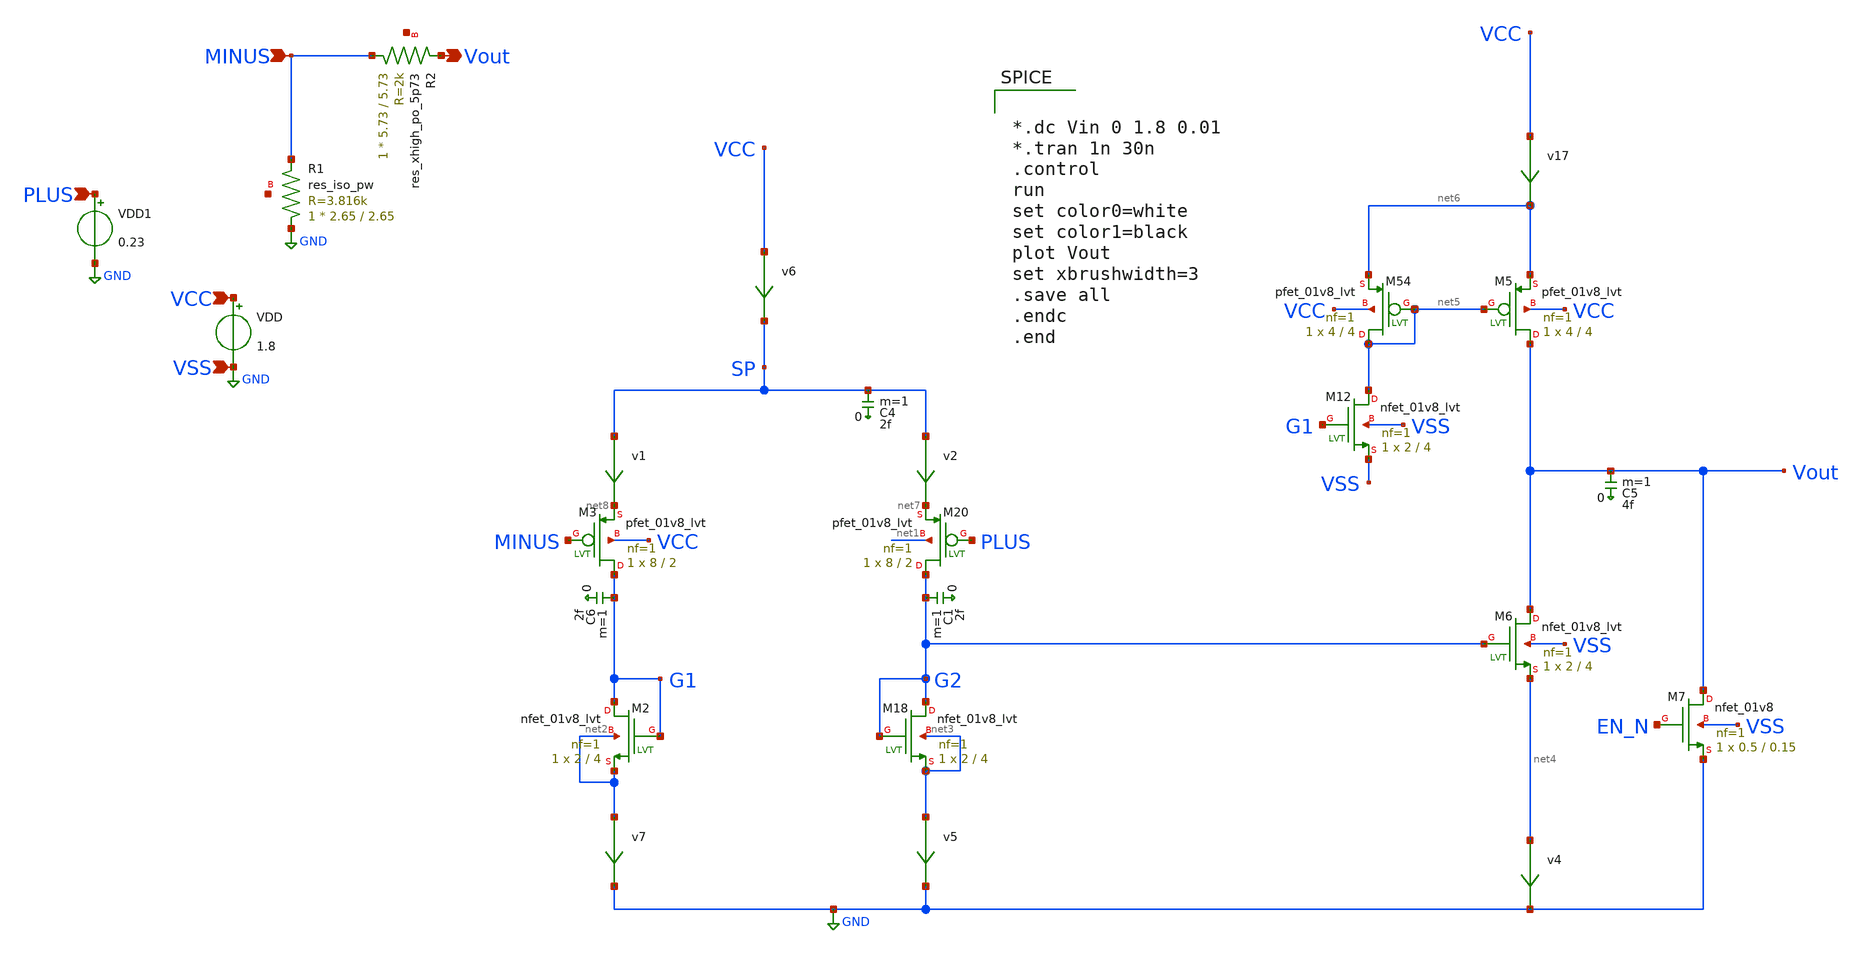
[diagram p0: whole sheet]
** sch_path: xschem/Vth_sch/Pre_layout/untitled.sch
**.subckt untitled PLUS MINUS VSS VCC Vout
*.ipin PLUS
*.ipin MINUS
*.ipin VSS
*.ipin VCC
*.opin Vout
C6 G1 0 2f m=1
XM18 G2 G2 net3 net3 sky130_fd_pr__nfet_01v8_lvt L=4 W=2 nf=1 ad='W * 0.29' as='W * 0.29' pd='2*(W + 0.29)'
+ ps='2*(W + 0.29)' nrd=0 nrs=0 sa=0 sb=0 sd=0 mult=1 m=1
XM2 G1 G1 net2 net2 sky130_fd_pr__nfet_01v8_lvt L=4 W=2 nf=1 ad='W * 0.29' as='W * 0.29' pd='2*(W + 0.29)'
+ ps='2*(W + 0.29)' nrd=0 nrs=0 sa=0 sb=0 sd=0 mult=1 m=1
XM20 G2 PLUS net7 net1 sky130_fd_pr__pfet_01v8_lvt L=2 W=8 nf=1 ad='W * 0.29' as='W * 0.29' pd='2*(W + 0.29)'
+ ps='2*(W + 0.29)' nrd=0 nrs=0 sa=0 sb=0 sd=0 mult=1 m=1
XM3 G1 MINUS net8 VCC sky130_fd_pr__pfet_01v8_lvt L=2 W=8 nf=1 ad='W * 0.29' as='W * 0.29' pd='2*(W + 0.29)'
+ ps='2*(W + 0.29)' nrd=0 nrs=0 sa=0 sb=0 sd=0 mult=1 m=1
v1 SP net8 0
.save i(v1)
C4 SP 0 2f m=1
C1 G2 0 2f m=1
C5 Vout 0 4f m=1
XM6 Vout G2 net4 VSS sky130_fd_pr__nfet_01v8_lvt L=4 W=2 nf=1 ad='W * 0.29' as='W * 0.29' pd='2*(W + 0.29)'
+ ps='2*(W + 0.29)' nrd=0 nrs=0 sa=0 sb=0 sd=0 mult=1 m=1
v2 SP net7 0
.save i(v2)
v4 net4 GND 0
.save i(v4)
v6 VCC SP 0
.save i(v6)
XM7 Vout EN_N GND VSS sky130_fd_pr__nfet_01v8 L=0.15 W=0.5 nf=1 ad='W * 0.29' as='W * 0.29' pd='2*(W + 0.29)'
+ ps='2*(W + 0.29)' nrd=0 nrs=0 sa=0 sb=0 sd=0 mult=1 m=1
v17 VCC net6 0
.save i(v17)
XM12 net5 G1 VSS VSS sky130_fd_pr__nfet_01v8_lvt L=4 W=2 nf=1 ad='W * 0.29' as='W * 0.29' pd='2*(W + 0.29)'
+ ps='2*(W + 0.29)' nrd=0 nrs=0 sa=0 sb=0 sd=0 mult=1 m=1
XM54 net5 net5 net6 VCC sky130_fd_pr__pfet_01v8_lvt L=4 W=4 nf=1 ad='W * 0.29' as='W * 0.29' pd='2*(W + 0.29)'
+ ps='2*(W + 0.29)' nrd=0 nrs=0 sa=0 sb=0 sd=0 mult=1 m=1
XM5 Vout net5 net6 VCC sky130_fd_pr__pfet_01v8_lvt L=4 W=4 nf=1 ad='W * 0.29' as='W * 0.29' pd='2*(W + 0.29)'
+ ps='2*(W + 0.29)' nrd=0 nrs=0 sa=0 sb=0 sd=0 mult=1 m=1
v5 net3 GND 0
.save i(v5)
v7 net2 GND 0
.save i(v7)
VDD VCC VSS 1.8
XR1 GND MINUS net9 sky130_fd_pr__res_iso_pw W=2.65 L=2.65 m=1
XR2 MINUS Vout net10 sky130_fd_pr__res_xhigh_po_5p73 L=5.73 mult=1 m=1
VDD1 PLUS GND 0.23
**** begin user architecture code


.lib /usr/local/share/pdk/sky130A/libs.tech/ngspice/sky130.lib.spice tt

.save all





*.dc Vin 0 1.8 0.01
*.tran 1n 30n
.control
run
set color0=white
set color1=black
plot Vout
set xbrushwidth=3
.save all
.endc
.end


**** end user architecture code
**.ends
.GLOBAL GND
.end
